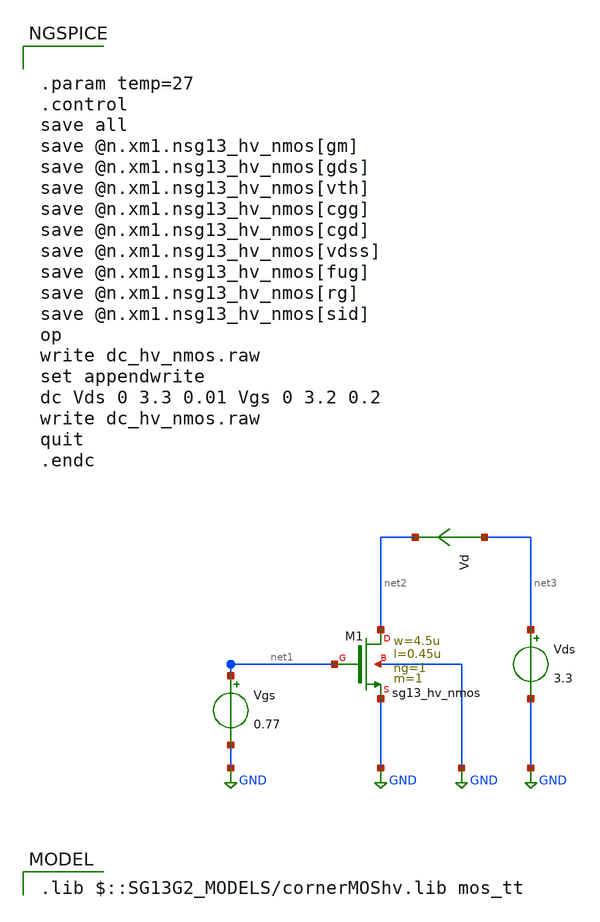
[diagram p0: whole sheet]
** sch_path: xschem/dc_hv_nmos.sch
* Copyright 2023-2024 IHP PDK Authors, Harald Pretl
**.subckt dc_hv_nmos
Vgs net1 GND 0.77
Vds net3 GND 3.3
Vd net3 net2 0
.save i(vd)
XM1 net2 net1 GND GND sg13_hv_nmos w=4.5u l=0.45u ng=1 m=1 mm_ok=1
**** begin user architecture code
 .lib $::SG13G2_MODELS/cornerMOShv.lib mos_tt



.param temp=27
.control
save all
save @n.xm1.nsg13_hv_nmos[gm]
save @n.xm1.nsg13_hv_nmos[gds]
save @n.xm1.nsg13_hv_nmos[vth]
save @n.xm1.nsg13_hv_nmos[cgg]
save @n.xm1.nsg13_hv_nmos[cgd]
save @n.xm1.nsg13_hv_nmos[vdss]
save @n.xm1.nsg13_hv_nmos[fug]
save @n.xm1.nsg13_hv_nmos[rg]
save @n.xm1.nsg13_hv_nmos[sid]
op
write dc_hv_nmos.raw
set appendwrite
dc Vds 0 3.3 0.01 Vgs 0 3.2 0.2
write dc_hv_nmos.raw
quit
.endc


**** end user architecture code
**.ends
.GLOBAL GND
.end
